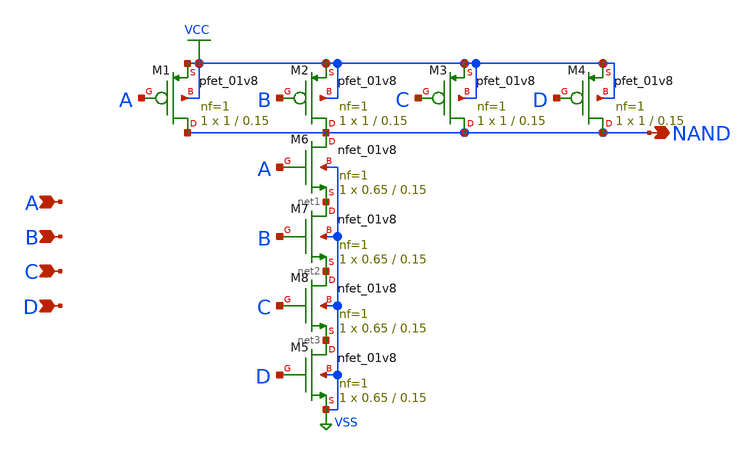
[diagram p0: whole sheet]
** sch_path: elements/nand4.sch
**.subckt nand4 A NAND B C D
*.ipin A
*.opin NAND
*.ipin B
*.ipin C
*.ipin D
XM1 NAND A VCC VCC sky130_fd_pr__pfet_01v8 L=0.15 W=1 nf=1 ad='int((nf+1)/2) * W/nf * 0.29' as='int((nf+2)/2) * W/nf * 0.29'
+ pd='2*int((nf+1)/2) * (W/nf + 0.29)' ps='2*int((nf+2)/2) * (W/nf + 0.29)' nrd='0.29 / W' nrs='0.29 / W'
+ sa=0 sb=0 sd=0 mult=1 m=1
XM2 NAND B VCC VCC sky130_fd_pr__pfet_01v8 L=0.15 W=1 nf=1 ad='int((nf+1)/2) * W/nf * 0.29' as='int((nf+2)/2) * W/nf * 0.29'
+ pd='2*int((nf+1)/2) * (W/nf + 0.29)' ps='2*int((nf+2)/2) * (W/nf + 0.29)' nrd='0.29 / W' nrs='0.29 / W'
+ sa=0 sb=0 sd=0 mult=1 m=1
XM3 NAND C VCC VCC sky130_fd_pr__pfet_01v8 L=0.15 W=1 nf=1 ad='int((nf+1)/2) * W/nf * 0.29' as='int((nf+2)/2) * W/nf * 0.29'
+ pd='2*int((nf+1)/2) * (W/nf + 0.29)' ps='2*int((nf+2)/2) * (W/nf + 0.29)' nrd='0.29 / W' nrs='0.29 / W'
+ sa=0 sb=0 sd=0 mult=1 m=1
XM6 NAND A net1 VSS sky130_fd_pr__nfet_01v8 L=0.15 W=0.65 nf=1 ad='int((1 + 1)/2) * 0.65 / 1 * 0.29'
+ as='int((1 + 2)/2) * 0.65 / 1 * 0.29' pd='2*int((1 + 1)/2) * (0.65 / 1 + 0.29)' ps='2*int((1 + 2)/2) * (0.65 / 1 + 0.29)'
+ nrd='0.29 / 0.65 ' nrs='0.29 / 0.65 ' sa=0 sb=0 sd=0 mult=1 m=1
XM7 net1 B net2 VSS sky130_fd_pr__nfet_01v8 L=0.15 W=0.65 nf=1 ad='int((1 + 1)/2) * 0.65 / 1 * 0.29'
+ as='int((1 + 2)/2) * 0.65 / 1 * 0.29' pd='2*int((1 + 1)/2) * (0.65 / 1 + 0.29)' ps='2*int((1 + 2)/2) * (0.65 / 1 + 0.29)'
+ nrd='0.29 / 0.65 ' nrs='0.29 / 0.65 ' sa=0 sb=0 sd=0 mult=1 m=1
XM8 net2 C net3 VSS sky130_fd_pr__nfet_01v8 L=0.15 W=0.65 nf=1 ad='int((1 + 1)/2) * 0.65 / 1 * 0.29'
+ as='int((1 + 2)/2) * 0.65 / 1 * 0.29' pd='2*int((1 + 1)/2) * (0.65 / 1 + 0.29)' ps='2*int((1 + 2)/2) * (0.65 / 1 + 0.29)'
+ nrd='0.29 / 0.65 ' nrs='0.29 / 0.65 ' sa=0 sb=0 sd=0 mult=1 m=1
XM4 NAND D VCC VCC sky130_fd_pr__pfet_01v8 L=0.15 W=1 nf=1 ad='int((nf+1)/2) * W/nf * 0.29' as='int((nf+2)/2) * W/nf * 0.29'
+ pd='2*int((nf+1)/2) * (W/nf + 0.29)' ps='2*int((nf+2)/2) * (W/nf + 0.29)' nrd='0.29 / W' nrs='0.29 / W'
+ sa=0 sb=0 sd=0 mult=1 m=1
XM5 net3 D VSS VSS sky130_fd_pr__nfet_01v8 L=0.15 W=0.65 nf=1 ad='int((1 + 1)/2) * 0.65 / 1 * 0.29' as='int((1 + 2)/2) * 0.65 / 1 * 0.29'
+ pd='2*int((1 + 1)/2) * (0.65 / 1 + 0.29)' ps='2*int((1 + 2)/2) * (0.65 / 1 + 0.29)' nrd='0.29 / 0.65 '
+ nrs='0.29 / 0.65 ' sa=0 sb=0 sd=0 mult=1 m=1
**.ends
.GLOBAL VCC
.GLOBAL VSS
.end
